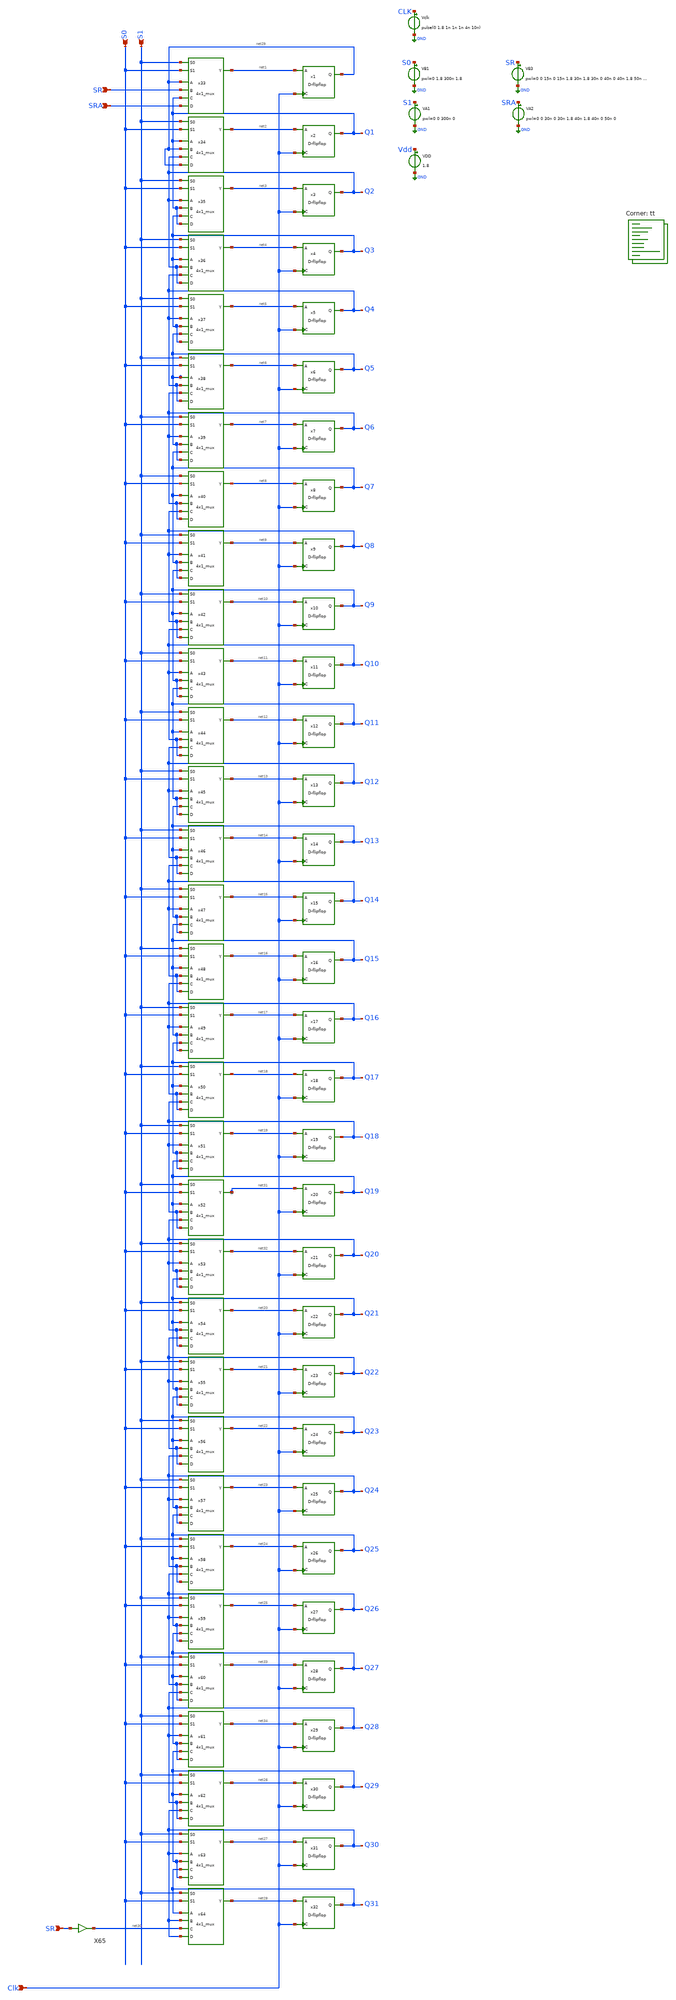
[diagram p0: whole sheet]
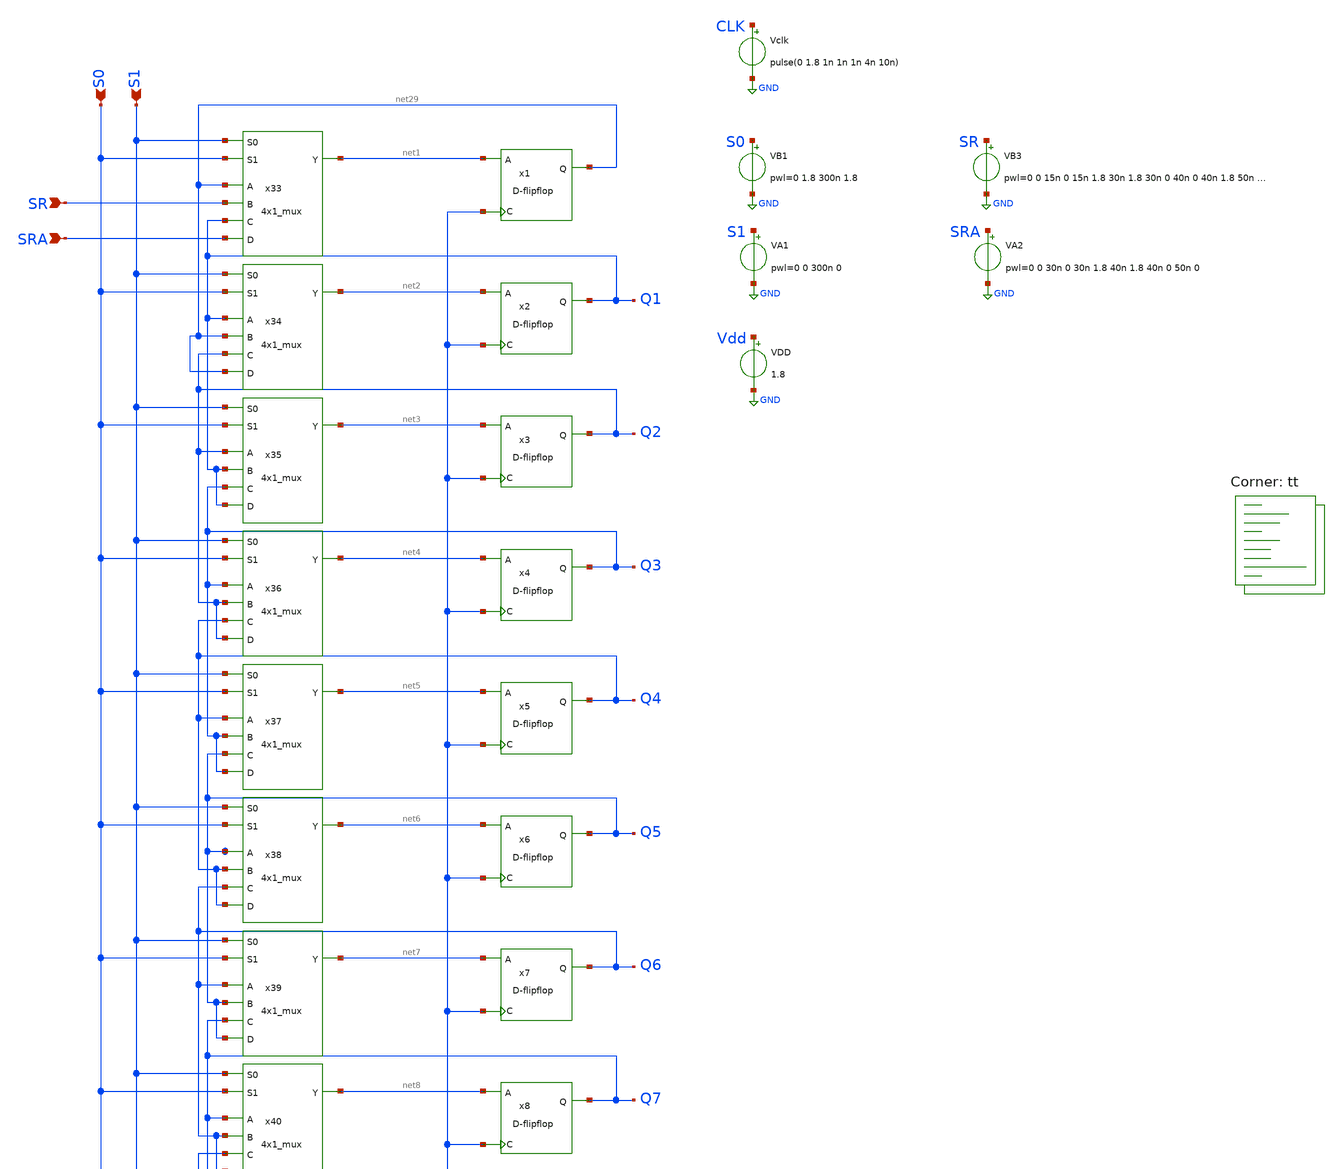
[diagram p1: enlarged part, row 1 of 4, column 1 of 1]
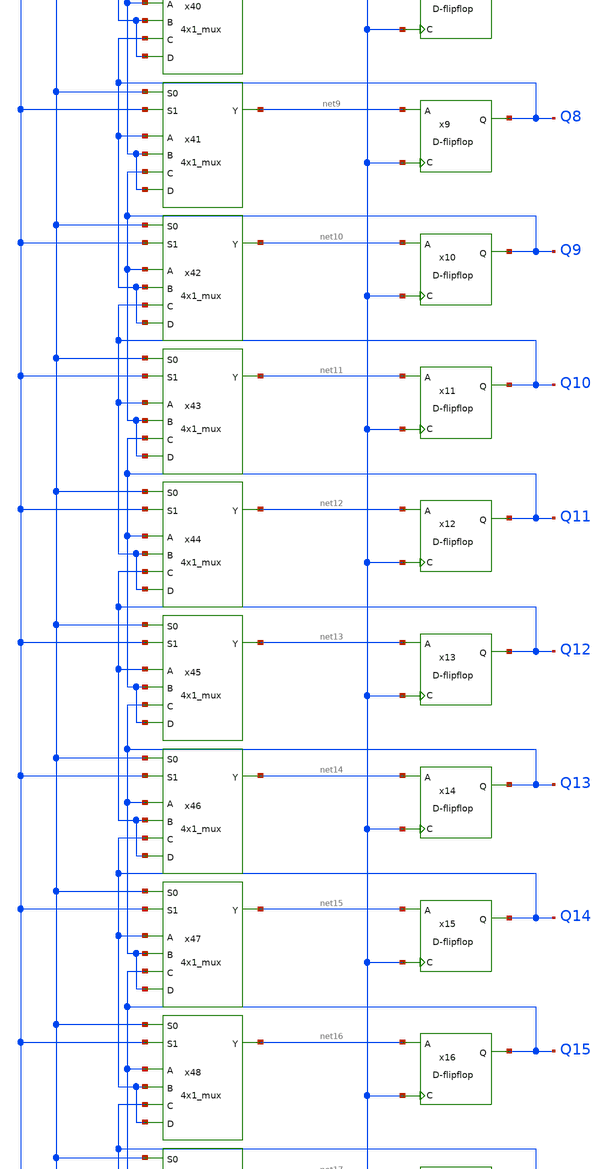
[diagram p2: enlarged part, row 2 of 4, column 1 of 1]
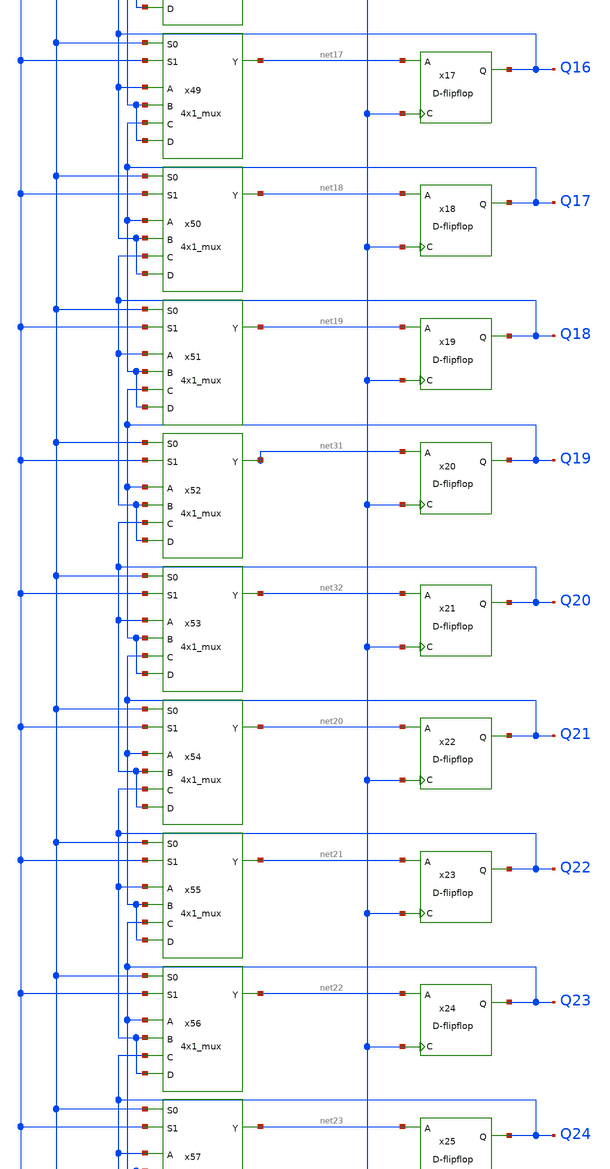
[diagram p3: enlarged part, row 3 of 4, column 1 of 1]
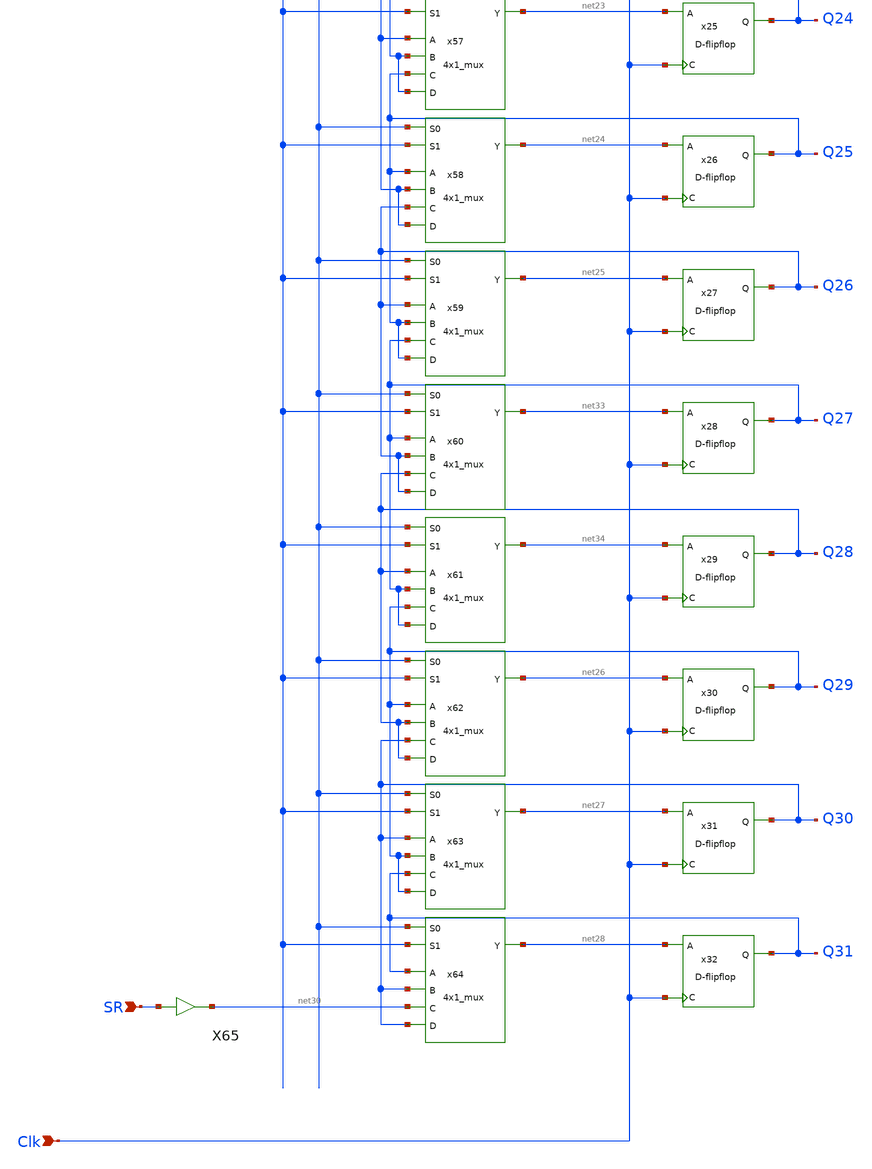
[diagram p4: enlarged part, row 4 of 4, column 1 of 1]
** sch_path: gates/32-bit shift.sch
**.subckt 32-bit shift S0 S1 SR Clk SR SRA
*.ipin S0
*.ipin S1
*.ipin SR
*.ipin Clk
*.ipin SR
*.ipin SRA
x1 net1 net29 Clk D-flipflop
x2 net2 Q1 Clk D-flipflop
x3 net3 Q2 Clk D-flipflop
x4 net4 Q3 Clk D-flipflop
x5 net5 Q4 Clk D-flipflop
x6 net6 Q5 Clk D-flipflop
x7 net7 Q6 Clk D-flipflop
x8 net8 Q7 Clk D-flipflop
x9 net9 Q8 Clk D-flipflop
x10 net10 Q9 Clk D-flipflop
x11 net11 Q10 Clk D-flipflop
x12 net12 Q11 Clk D-flipflop
x13 net13 Q12 Clk D-flipflop
x14 net14 Q13 Clk D-flipflop
x15 net15 Q14 Clk D-flipflop
x16 net16 Q15 Clk D-flipflop
x17 net17 Q16 Clk D-flipflop
x18 net18 Q17 Clk D-flipflop
x19 net19 Q18 Clk D-flipflop
x20 net31 Q19 Clk D-flipflop
x21 net32 Q20 Clk D-flipflop
x22 net20 Q21 Clk D-flipflop
x23 net21 Q22 Clk D-flipflop
x24 net22 Q23 Clk D-flipflop
x25 net23 Q24 Clk D-flipflop
x26 net24 Q25 Clk D-flipflop
x27 net25 Q26 Clk D-flipflop
x28 net33 Q27 Clk D-flipflop
x29 net34 Q28 Clk D-flipflop
x30 net26 Q29 Clk D-flipflop
x31 net27 Q30 Clk D-flipflop
x32 net28 Q31 Clk D-flipflop
x33 net29 SR net1 Q1 SRA S1 S0 4x1_mux
x34 Q1 net29 net2 Q2 net29 S1 S0 4x1_mux
x35 Q2 Q1 net3 Q3 Q1 S1 S0 4x1_mux
x36 Q3 Q2 net4 Q4 Q2 S1 S0 4x1_mux
x37 Q4 Q3 net5 Q5 Q3 S1 S0 4x1_mux
x38 Q5 Q4 net6 Q6 Q4 S1 S0 4x1_mux
x39 Q6 Q5 net7 Q7 Q5 S1 S0 4x1_mux
x40 Q7 Q6 net8 Q8 Q6 S1 S0 4x1_mux
x41 Q8 Q7 net9 Q9 Q7 S1 S0 4x1_mux
x42 Q9 Q8 net10 Q10 Q8 S1 S0 4x1_mux
x43 Q10 Q9 net11 Q11 Q9 S1 S0 4x1_mux
x44 Q11 Q10 net12 Q12 Q10 S1 S0 4x1_mux
x45 Q12 Q11 net13 Q13 Q11 S1 S0 4x1_mux
x46 Q13 Q12 net14 Q14 Q12 S1 S0 4x1_mux
x47 Q14 Q13 net15 Q15 Q13 S1 S0 4x1_mux
x48 Q15 Q14 net16 Q16 Q14 S1 S0 4x1_mux
x49 Q16 Q15 net17 Q17 Q15 S1 S0 4x1_mux
x50 Q17 Q16 net18 Q18 Q16 S1 S0 4x1_mux
x51 Q18 Q17 net19 Q19 Q17 S1 S0 4x1_mux
x52 Q19 Q18 net31 Q20 Q18 S1 S0 4x1_mux
x53 Q20 Q19 net32 Q21 Q19 S1 S0 4x1_mux
x54 Q21 Q20 net20 Q22 Q20 S1 S0 4x1_mux
x55 Q22 Q21 net21 Q23 Q21 S1 S0 4x1_mux
x56 Q23 Q22 net22 Q24 Q22 S1 S0 4x1_mux
x57 Q24 Q23 net23 Q25 Q23 S1 S0 4x1_mux
x58 Q25 Q24 net24 Q26 Q24 S1 S0 4x1_mux
x59 Q26 Q25 net25 Q27 Q25 S1 S0 4x1_mux
x60 Q27 Q26 net33 Q28 Q26 S1 S0 4x1_mux
x61 Q28 Q27 net34 Q29 Q27 S1 S0 4x1_mux
x62 Q29 Q28 net26 Q30 Q28 S1 S0 4x1_mux
x63 Q30 Q29 net27 Q31 Q29 S1 S0 4x1_mux
x64 Q31 Q30 net28 net30 Q30 S1 S0 4x1_mux
VDD Vdd GND 1.8
VA1 S1 GND pwl=0 0 300n 0
VB1 S0 GND pwl=0 1.8 300n 1.8
Vclk CLK GND pulse(0 1.8 1n 1n 1n 4n 10n)
VA2 SRA GND pwl=0 0 30n 0 30n 1.8 40n 1.8 40n 0 50n 0
VB3 SR GND pwl=0 0 15n 0 15n 1.8 30n 1.8 30n 0 40n 0 40n 1.8 50n 1.8 50n 0 150n 0 150n 1.8 180n 1.8
+ 300n 1.8 300n 0
X65 SR net30 inv_vtc
**** begin user architecture code

.ic v(net29)=0 v(Q1)=0 v(Q2)=0 v(Q3)=0 v(Q4)=0 v(Q5)=0 v(Q6)=0 v(Q7)=0 v(Q8)=0 v(Q9)=0 v(Q10)=0
+ v(Q11)=0 v(Q12)=0 v(Q13)=0 v(Q14)=0 v(Q15)=0 v(Q16)=0 v(Q17)=0 v(Q18)=0 v(Q19)=0 v(Q20)=0 v(Q21)=0 v(Q22)=0
+ v(Q23)=0 v(Q0)=0 v(Q24)=0 v(Q25)=0 v(Q26)=0 v(Q27)=0 v(Q28)=0 v(Q29)=0 v(Q30)=0 v(Q31)=0
.tran 0.01n 350n
.save all

.lib $::SKYWATER_MODELS/sky130.lib.spice tt
**** end user architecture code
**.ends

* expanding   symbol:  D-flipflop.sym # of pins=3
** sym_path: gates/D-flipflop.sym
** sch_path: gates/D-flipflop.sch
.subckt D-flipflop A Q C
*.ipin A
*.ipin C
*.opin Q
x1 A net1 C NAND2_Gate
x2 net3 net2 C NAND2_Gate
x3 net1 Q Q' NAND2_Gate
x4 net2 Q' Q NAND2_Gate
X5 A net3 inv_vtc
.ends


* expanding   symbol:  4x1_mux.sym # of pins=7
** sym_path: gates/4x1_mux.sym
** sch_path: gates/4x1_mux.sch
.subckt 4x1_mux A B Y C D S0 S1
*.ipin A
*.ipin B
*.ipin C
*.ipin D
*.ipin S0
*.ipin S1
*.opin Y
x1 net1 A net5 net6 VCC VSS VCC VSS AND3
x2 net2 B net5 S1 VCC VSS VCC VSS AND3
x3 net3 C S0 net6 VCC VSS VCC VSS AND3
x4 net4 D S0 S0 VCC VSS VCC VSS AND3
x5 net1 net2 net3 Y net4 OR4
X6 S0 net5 inv_vtc
X7 S1 net6 inv_vtc
.ends


* expanding   symbol:  /home/apn/test_xschem_sky130/inv_vtc.sym # of pins=2
** sym_path: gates/inv_vtc.sym
** sch_path: gates/inv_vtc.sch
.subckt inv_vtc A Y
*.ipin A
*.opin Y
XM1 Y A VDD VDD sky130_fd_pr__pfet_01v8 L=0.15 W=2 nf=1 ad='int((nf+1)/2) * W/nf * 0.29' as='int((nf+2)/2) * W/nf * 0.29'
+ pd='2*int((nf+1)/2) * (W/nf + 0.29)' ps='2*int((nf+2)/2) * (W/nf + 0.29)' nrd='0.29 / W' nrs='0.29 / W'
+ sa=0 sb=0 sd=0 mult=1 m=1
XM2 Y A GND GND sky130_fd_pr__nfet_01v8 L=0.15 W=1 nf=1 ad='int((nf+1)/2) * W/nf * 0.29' as='int((nf+2)/2) * W/nf * 0.29'
+ pd='2*int((nf+1)/2) * (W/nf + 0.29)' ps='2*int((nf+2)/2) * (W/nf + 0.29)' nrd='0.29 / W' nrs='0.29 / W'
+ sa=0 sb=0 sd=0 mult=1 m=1
.ends


* expanding   symbol:  NAND2_Gate.sym # of pins=3
** sym_path: gates/NAND2_Gate.sym
** sch_path: gates/NAND2_Gate.sch
.subckt NAND2_Gate A Y B
*.ipin A
*.ipin B
*.opin Y
XM1 Y A net1 GND sky130_fd_pr__nfet_01v8 L=0.15 W=1 nf=1 ad='int((nf+1)/2) * W/nf * 0.29' as='int((nf+2)/2) * W/nf * 0.29'
+ pd='2*int((nf+1)/2) * (W/nf + 0.29)' ps='2*int((nf+2)/2) * (W/nf + 0.29)' nrd='0.29 / W' nrs='0.29 / W'
+ sa=0 sb=0 sd=0 mult=1 m=1
XM2 net1 B GND GND sky130_fd_pr__nfet_01v8 L=0.15 W=1 nf=1 ad='int((nf+1)/2) * W/nf * 0.29' as='int((nf+2)/2) * W/nf * 0.29'
+ pd='2*int((nf+1)/2) * (W/nf + 0.29)' ps='2*int((nf+2)/2) * (W/nf + 0.29)' nrd='0.29 / W' nrs='0.29 / W'
+ sa=0 sb=0 sd=0 mult=1 m=1
XM3 Y A VDD VDD sky130_fd_pr__pfet_01v8 L=0.15 W=1 nf=1 ad='int((nf+1)/2) * W/nf * 0.29' as='int((nf+2)/2) * W/nf * 0.29'
+ pd='2*int((nf+1)/2) * (W/nf + 0.29)' ps='2*int((nf+2)/2) * (W/nf + 0.29)' nrd='0.29 / W' nrs='0.29 / W'
+ sa=0 sb=0 sd=0 mult=1 m=1
XM4 Y B VDD VDD sky130_fd_pr__pfet_01v8 L=0.15 W=1 nf=1 ad='int((nf+1)/2) * W/nf * 0.29' as='int((nf+2)/2) * W/nf * 0.29'
+ pd='2*int((nf+1)/2) * (W/nf + 0.29)' ps='2*int((nf+2)/2) * (W/nf + 0.29)' nrd='0.29 / W' nrs='0.29 / W'
+ sa=0 sb=0 sd=0 mult=1 m=1
.ends


* expanding   symbol:  OR4.sym # of pins=5
** sym_path: gates/OR4.sym
** sch_path: gates/OR4.sch
.subckt OR4 D C B Y A
*.ipin A
*.ipin B
*.opin Y
*.ipin C
*.ipin D
XM2 GND D net1 GND sky130_fd_pr__nfet_01v8 L=0.15 W=1 nf=1 ad='int((nf+1)/2) * W/nf * 0.29' as='int((nf+2)/2) * W/nf * 0.29'
+ pd='2*int((nf+1)/2) * (W/nf + 0.29)' ps='2*int((nf+2)/2) * (W/nf + 0.29)' nrd='0.29 / W' nrs='0.29 / W'
+ sa=0 sb=0 sd=0 mult=1 m=1
XM4 VDD D net4 VDD sky130_fd_pr__pfet_01v8 L=0.15 W=1 nf=1 ad='int((nf+1)/2) * W/nf * 0.29' as='int((nf+2)/2) * W/nf * 0.29'
+ pd='2*int((nf+1)/2) * (W/nf + 0.29)' ps='2*int((nf+2)/2) * (W/nf + 0.29)' nrd='0.29 / W' nrs='0.29 / W'
+ sa=0 sb=0 sd=0 mult=1 m=1
XM5 net4 C net3 VDD sky130_fd_pr__pfet_01v8 L=0.15 W=1 nf=1 ad='int((nf+1)/2) * W/nf * 0.29' as='int((nf+2)/2) * W/nf * 0.29'
+ pd='2*int((nf+1)/2) * (W/nf + 0.29)' ps='2*int((nf+2)/2) * (W/nf + 0.29)' nrd='0.29 / W' nrs='0.29 / W'
+ sa=0 sb=0 sd=0 mult=1 m=1
XM6 GND C net1 GND sky130_fd_pr__nfet_01v8 L=0.15 W=1 nf=1 ad='int((nf+1)/2) * W/nf * 0.29' as='int((nf+2)/2) * W/nf * 0.29'
+ pd='2*int((nf+1)/2) * (W/nf + 0.29)' ps='2*int((nf+2)/2) * (W/nf + 0.29)' nrd='0.29 / W' nrs='0.29 / W'
+ sa=0 sb=0 sd=0 mult=1 m=1
XM7 net3 B net2 VDD sky130_fd_pr__pfet_01v8 L=0.15 W=1 nf=1 ad='int((nf+1)/2) * W/nf * 0.29' as='int((nf+2)/2) * W/nf * 0.29'
+ pd='2*int((nf+1)/2) * (W/nf + 0.29)' ps='2*int((nf+2)/2) * (W/nf + 0.29)' nrd='0.29 / W' nrs='0.29 / W'
+ sa=0 sb=0 sd=0 mult=1 m=1
XM8 GND B net1 GND sky130_fd_pr__nfet_01v8 L=0.15 W=1 nf=1 ad='int((nf+1)/2) * W/nf * 0.29' as='int((nf+2)/2) * W/nf * 0.29'
+ pd='2*int((nf+1)/2) * (W/nf + 0.29)' ps='2*int((nf+2)/2) * (W/nf + 0.29)' nrd='0.29 / W' nrs='0.29 / W'
+ sa=0 sb=0 sd=0 mult=1 m=1
XM9 net2 A net1 VDD sky130_fd_pr__pfet_01v8 L=0.15 W=1 nf=1 ad='int((nf+1)/2) * W/nf * 0.29' as='int((nf+2)/2) * W/nf * 0.29'
+ pd='2*int((nf+1)/2) * (W/nf + 0.29)' ps='2*int((nf+2)/2) * (W/nf + 0.29)' nrd='0.29 / W' nrs='0.29 / W'
+ sa=0 sb=0 sd=0 mult=1 m=1
XM10 GND A net1 GND sky130_fd_pr__nfet_01v8 L=0.15 W=1 nf=1 ad='int((nf+1)/2) * W/nf * 0.29' as='int((nf+2)/2) * W/nf * 0.29'
+ pd='2*int((nf+1)/2) * (W/nf + 0.29)' ps='2*int((nf+2)/2) * (W/nf + 0.29)' nrd='0.29 / W' nrs='0.29 / W'
+ sa=0 sb=0 sd=0 mult=1 m=1
X2 net1 Y inv_vtc
.ends

.GLOBAL GND
.GLOBAL VDD
.end
